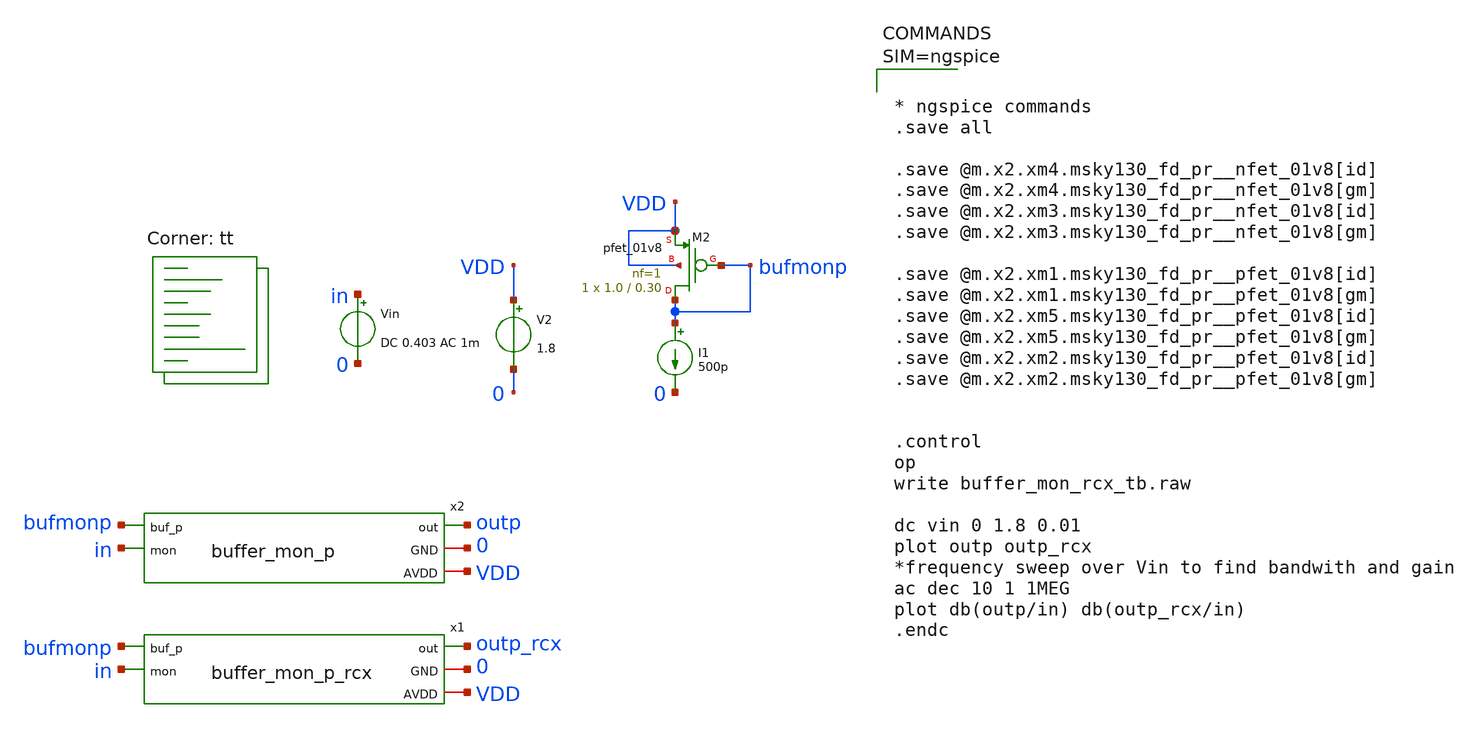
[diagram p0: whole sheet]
** sch_path: design/xschem/layout_tb/buffer_mon_p_rcx_tb.sch
**.subckt buffer_mon_p_rcx_tb
x1 bufmonp outp_rcx in 0 VDD buffer_mon_p_rcx
V2 VDD 0 1.8
Vin in 0 DC 0.403 AC 1m
x2 bufmonp outp in 0 VDD buffer_mon_p
I1 bufmonp 0 500p
XM2 bufmonp bufmonp VDD VDD sky130_fd_pr__pfet_01v8 L=0.30 W=1.0 nf=1 ad='int((nf+1)/2) * W/nf * 0.29'
+ as='int((nf+2)/2) * W/nf * 0.29' pd='2*int((nf+1)/2) * (W/nf + 0.29)' ps='2*int((nf+2)/2) * (W/nf + 0.29)'
+ nrd='0.29 / W' nrs='0.29 / W' sa=0 sb=0 sd=0 mult=1 m=1
**** begin user architecture code
.lib $::SKYWATER_MODELS/sky130.lib.spice tt



* ngspice commands
.save all

.save @m.x2.xm4.msky130_fd_pr__nfet_01v8[id]
.save @m.x2.xm4.msky130_fd_pr__nfet_01v8[gm]
.save @m.x2.xm3.msky130_fd_pr__nfet_01v8[id]
.save @m.x2.xm3.msky130_fd_pr__nfet_01v8[gm]

.save @m.x2.xm1.msky130_fd_pr__pfet_01v8[id]
.save @m.x2.xm1.msky130_fd_pr__pfet_01v8[gm]
.save @m.x2.xm5.msky130_fd_pr__pfet_01v8[id]
.save @m.x2.xm5.msky130_fd_pr__pfet_01v8[gm]
.save @m.x2.xm2.msky130_fd_pr__pfet_01v8[id]
.save @m.x2.xm2.msky130_fd_pr__pfet_01v8[gm]


.control
op
write buffer_mon_rcx_tb.raw

dc vin 0 1.8 0.01
plot outp outp_rcx
*frequency sweep over Vin to find bandwith and gain
ac dec 10 1 1MEG
plot db(outp/in) db(outp_rcx/in)
.endc



**** end user architecture code
**.ends

* expanding   symbol:  buffer_mon_p_rcx.sym # of pins=5
** sym_path: design/xschem/buffer_mon_p.sym
.include [abs_sym_path buffer_mon_p_rcx.spice]

* expanding   symbol:  buffer_mon_p.sym # of pins=5
** sym_path: design/xschem/buffer_mon_p.sym
** sch_path: design/xschem/buffer_mon_p.sch
.subckt buffer_mon_p buf_p out mon GND AVDD
*.iopin GND
*.iopin AVDD
*.ipin buf_p
*.ipin mon
*.opin out
XM1 out out net2 AVDD sky130_fd_pr__pfet_01v8 L=0.5 W=1.0 nf=1 ad='int((nf+1)/2) * W/nf * 0.29' as='int((nf+2)/2) * W/nf * 0.29'
+ pd='2*int((nf+1)/2) * (W/nf + 0.29)' ps='2*int((nf+2)/2) * (W/nf + 0.29)' nrd='0.29 / W' nrs='0.29 / W'
+ sa=0 sb=0 sd=0 mult=1 m=1
XM5 net1 mon net2 AVDD sky130_fd_pr__pfet_01v8 L=0.5 W=1.0 nf=1 ad='int((nf+1)/2) * W/nf * 0.29' as='int((nf+2)/2) * W/nf * 0.29'
+ pd='2*int((nf+1)/2) * (W/nf + 0.29)' ps='2*int((nf+2)/2) * (W/nf + 0.29)' nrd='0.29 / W' nrs='0.29 / W'
+ sa=0 sb=0 sd=0 mult=1 m=1
XM2 net2 buf_p AVDD AVDD sky130_fd_pr__pfet_01v8 L=0.30 W=1.0 nf=1 ad='int((nf+1)/2) * W/nf * 0.29' as='int((nf+2)/2) * W/nf * 0.29'
+ pd='2*int((nf+1)/2) * (W/nf + 0.29)' ps='2*int((nf+2)/2) * (W/nf + 0.29)' nrd='0.29 / W' nrs='0.29 / W'
+ sa=0 sb=0 sd=0 mult=1 m=1
XM3 out net1 GND GND sky130_fd_pr__nfet_01v8 L=0.5 W=1.0 nf=1 ad='int((nf+1)/2) * W/nf * 0.29' as='int((nf+2)/2) * W/nf * 0.29'
+ pd='2*int((nf+1)/2) * (W/nf + 0.29)' ps='2*int((nf+2)/2) * (W/nf + 0.29)' nrd='0.29 / W' nrs='0.29 / W'
+ sa=0 sb=0 sd=0 mult=1 m=1
XM4 net1 net1 GND GND sky130_fd_pr__nfet_01v8 L=0.5 W=1.0 nf=1 ad='int((nf+1)/2) * W/nf * 0.29' as='int((nf+2)/2) * W/nf * 0.29'
+ pd='2*int((nf+1)/2) * (W/nf + 0.29)' ps='2*int((nf+2)/2) * (W/nf + 0.29)' nrd='0.29 / W' nrs='0.29 / W'
+ sa=0 sb=0 sd=0 mult=1 m=1
.ends

.end
